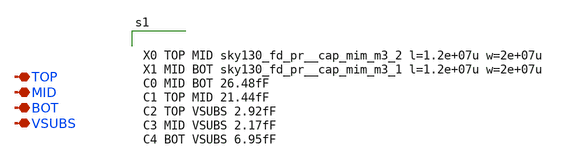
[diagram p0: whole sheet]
** sch_path: xschem/untitled-11.sch
**.subckt untitled-11 TOP MID BOT VSUBS
*.iopin TOP
*.iopin MID
*.iopin BOT
*.iopin VSUBS
**** begin user architecture code


X0 TOP MID sky130_fd_pr__cap_mim_m3_2 l=1.2e+07u w=2e+07u
X1 MID BOT sky130_fd_pr__cap_mim_m3_1 l=1.2e+07u w=2e+07u
C0 MID BOT 26.48fF
C1 TOP MID 21.44fF
C2 TOP VSUBS 2.92fF
C3 MID VSUBS 2.17fF
C4 BOT VSUBS 6.95fF



**** end user architecture code
**.ends
.end
